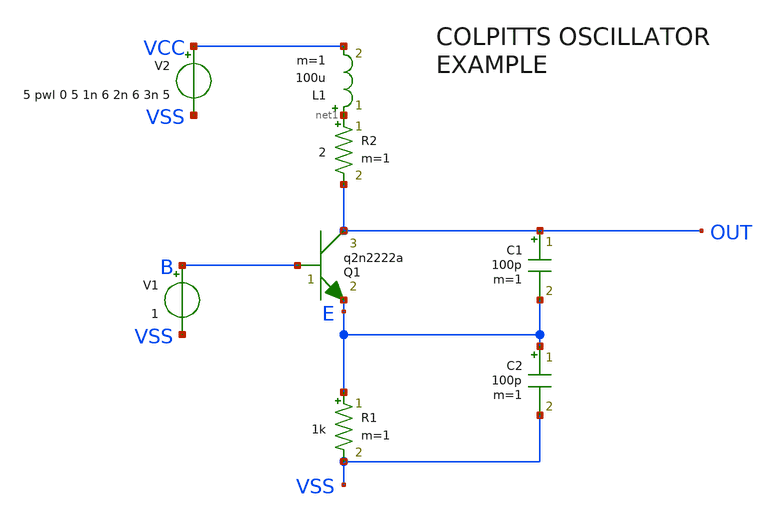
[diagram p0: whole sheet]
** sch_path: tests/test_sweep_diff/examples/osc/schematic/osc.sch
* Copyright (C) 1998-2024 Stefan Frederik Schippers
* This program is free software; you can redistribute it and/or modify
* it under the terms of the GNU General Public License as published by
* the Free Software Foundation; either version 2 of the License, or
* (at your option) any later version.
* This program is distributed in the hope that it will be useful,
* but WITHOUT ANY WARRANTY; without even the implied warranty of
* MERCHANTABILITY or FITNESS FOR A PARTICULAR PURPOSE.  See the
* GNU General Public License for more details.
* You should have received a copy of the GNU General Public License
* along with this program; if not, write to the Free Software
**.subckt osc
Q1 OUT B E q2n2222a area=1 m=1
V2 VCC VSS 5 pwl 0 5 1n 6 2n 6 3n 5
L1 net1 VCC 100u m=1
C1 OUT E 100p m=1
V1 B VSS 1
R1 E VSS 1k m=1
R2 net1 OUT 2 m=1
C2 E VSS 100p m=1
**** begin user architecture code

.option RUNLVL=6 post
vvss vss 0 dc 0
.save all
.temp 30

** models are generally not free: you must download
** SPICE models for active devices
** (https://www.centralsemi.com/docs/csm/2N2222A.LIB)
** and put them  into the below
** referenced file in simulation directory.
.include "models_osc.txt"


.tran 1n 100u
.probe tran i1(Q1) i2(Q1) i3(Q1) i(L1) i(c1) i(c2) i(r1) i(r2) i(r3)


**** end user architecture code
**.ends
.end
